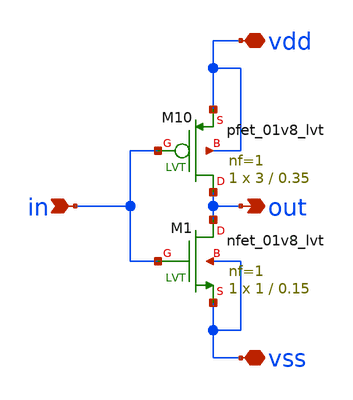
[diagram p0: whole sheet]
** sch_path: xschem/symbols/sky130A_01v8lvt_inv1.sch
* Copyright 2021 Stefan Frederik Schippers
* Licensed under the Apache License, Version 2.0 (the "License");
* you may not use this file except in compliance with the License.
* You may obtain a copy of the License at
* https://www.apache.org/licenses/LICENSE-2.0
* Unless required by applicable law or agreed to in writing, software
* distributed under the License is distributed on an "AS IS" BASIS,
* WITHOUT WARRANTIES OR CONDITIONS OF ANY KIND, either express or implied.
* See the License for the specific language governing permissions and
* limitations under the License.
**.subckt sky130A_01v8lvt_inv1 vdd vss in out
*.iopin vdd
*.iopin vss
*.ipin in
*.opin out
XM1 out in vss vss sky130_fd_pr__nfet_01v8_lvt L=0.15 W=1 nf=1 ad='int((1 + 1)/2) * 1 / 1 * 0.29' as='int((1 + 2)/2) * 1 / 1 * 0.29'
+ pd='2*int((1 + 1)/2) * (1 / 1 + 0.29)' ps='2*int((1 + 2)/2) * (1 / 1 + 0.29)' nrd='0.29 / 1 ' nrs='0.29 / 1 '
+ sa=0 sb=0 sd=0 mult=1 m=1
XM10 out in vdd vdd sky130_fd_pr__pfet_01v8_lvt L=0.35 W=3 nf=1 ad='int((1 + 1)/2) * 3 / 1 * 0.29' as='int((1 + 2)/2) * 3 / 1 * 0.29'
+ pd='2*int((1 + 1)/2) * (3 / 1 + 0.29)' ps='2*int((1 + 2)/2) * (3 / 1 + 0.29)' nrd='0.29 / 3 ' nrs='0.29 / 3 '
+ sa=0 sb=0 sd=0 mult=1 m=1
**.ends
.end
